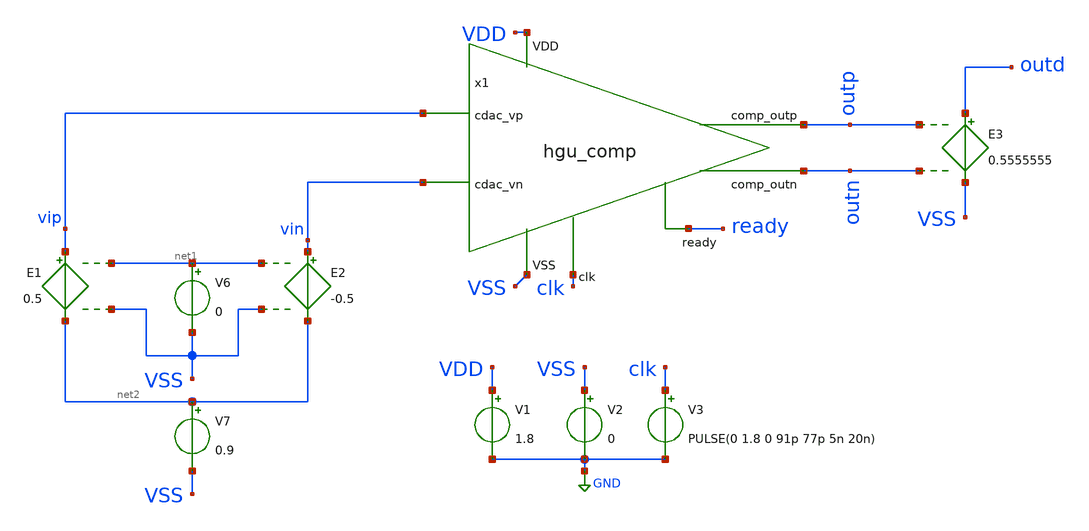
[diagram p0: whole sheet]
** sch_path: hgu/tb/tb_hgu_comp_MC_sim.sch
**.subckt tb_hgu_comp_MC_sim
x1 ready vin outp outn vip clk VDD VSS hgu_comp
V1 VDD GND 1.8
V2 VSS GND 0
V3 clk GND PULSE(0 1.8 0 91p 77p 5n 20n)
E1 vip net2 net1 VSS 0.5
E2 vin net2 net1 VSS -0.5
V6 net1 VSS 0
V7 net2 VSS 0.9
E3 outd VSS outp outn 0.5555555
**** begin user architecture code



.include /foss/designs/hgu_goss/hgu/spice/hgu_comp_flat_RC.spice
.lib /foss/pdks/sky130A/libs.tech/ngspice/sky130.lib.spice tt_mm
.include /foss/pdks/sky130A/libs.ref/sky130_fd_sc_hd/spice/sky130_fd_sc_hd.spice
.tran 0.1ns 100ns
.temp 25
.control
    repeat 20

    tran 0.1ns 100ns
    write test_mc_model.txt
    set appendwrite
    print V(outd)
    reset

    end
    plot all.v(outd)
.endc
.save all
.save all


**** end user architecture code
**.ends

* expanding   symbol:  ../xschem/hgu_comp.sym # of pins=8
** sym_path: hgu/xschem/hgu_comp.sym
** sch_path: hgu/xschem/hgu_comp.sch
.subckt hgu_comp ready cdac_vn comp_outp comp_outn cdac_vp clk VDD VSS
*.ipin cdac_vn
*.ipin cdac_vp
*.ipin VSS
*.ipin VDD
*.ipin clk
*.opin ready
*.opin comp_outp
*.opin comp_outn
XM1 net1 clk VSS VSS sky130_fd_pr__nfet_01v8 L=0.15 W=4 nf=4 ad='int((nf+1)/2) * W/nf * 0.29' as='int((nf+2)/2) * W/nf * 0.29'
+ pd='2*int((nf+1)/2) * (W/nf + 0.29)' ps='2*int((nf+2)/2) * (W/nf + 0.29)' nrd='0.29 / W' nrs='0.29 / W'
+ sa=0 sb=0 sd=0 mult=1 m=1
XM4 Y X Q VSS sky130_fd_pr__nfet_01v8 L=0.15 W=1 nf=1 ad='int((nf+1)/2) * W/nf * 0.29' as='int((nf+2)/2) * W/nf * 0.29'
+ pd='2*int((nf+1)/2) * (W/nf + 0.29)' ps='2*int((nf+2)/2) * (W/nf + 0.29)' nrd='0.29 / W' nrs='0.29 / W'
+ sa=0 sb=0 sd=0 mult=1 m=1
XM5 X Y P VSS sky130_fd_pr__nfet_01v8 L=0.15 W=1 nf=1 ad='int((nf+1)/2) * W/nf * 0.29' as='int((nf+2)/2) * W/nf * 0.29'
+ pd='2*int((nf+1)/2) * (W/nf + 0.29)' ps='2*int((nf+2)/2) * (W/nf + 0.29)' nrd='0.29 / W' nrs='0.29 / W'
+ sa=0 sb=0 sd=0 mult=1 m=1
XM6 X Y VDD VDD sky130_fd_pr__pfet_01v8 L=0.15 W=1 nf=1 ad='int((nf+1)/2) * W/nf * 0.29' as='int((nf+2)/2) * W/nf * 0.29'
+ pd='2*int((nf+1)/2) * (W/nf + 0.29)' ps='2*int((nf+2)/2) * (W/nf + 0.29)' nrd='0.29 / W' nrs='0.29 / W'
+ sa=0 sb=0 sd=0 mult=1 m=1
XM7 Y X VDD VDD sky130_fd_pr__pfet_01v8 L=0.15 W=1 nf=1 ad='int((nf+1)/2) * W/nf * 0.29' as='int((nf+2)/2) * W/nf * 0.29'
+ pd='2*int((nf+1)/2) * (W/nf + 0.29)' ps='2*int((nf+2)/2) * (W/nf + 0.29)' nrd='0.29 / W' nrs='0.29 / W'
+ sa=0 sb=0 sd=0 mult=1 m=1
XM8 X clk VDD VDD sky130_fd_pr__pfet_01v8 L=0.15 W=1 nf=1 ad='int((nf+1)/2) * W/nf * 0.29' as='int((nf+2)/2) * W/nf * 0.29'
+ pd='2*int((nf+1)/2) * (W/nf + 0.29)' ps='2*int((nf+2)/2) * (W/nf + 0.29)' nrd='0.29 / W' nrs='0.29 / W'
+ sa=0 sb=0 sd=0 mult=1 m=1
XM9 P clk VDD VDD sky130_fd_pr__pfet_01v8 L=0.15 W=1 nf=1 ad='int((nf+1)/2) * W/nf * 0.29' as='int((nf+2)/2) * W/nf * 0.29'
+ pd='2*int((nf+1)/2) * (W/nf + 0.29)' ps='2*int((nf+2)/2) * (W/nf + 0.29)' nrd='0.29 / W' nrs='0.29 / W'
+ sa=0 sb=0 sd=0 mult=1 m=1
XM10 Y clk VDD VDD sky130_fd_pr__pfet_01v8 L=0.15 W=1 nf=1 ad='int((nf+1)/2) * W/nf * 0.29' as='int((nf+2)/2) * W/nf * 0.29'
+ pd='2*int((nf+1)/2) * (W/nf + 0.29)' ps='2*int((nf+2)/2) * (W/nf + 0.29)' nrd='0.29 / W' nrs='0.29 / W'
+ sa=0 sb=0 sd=0 mult=1 m=1
XM11 Q clk VDD VDD sky130_fd_pr__pfet_01v8 L=0.15 W=1 nf=1 ad='int((nf+1)/2) * W/nf * 0.29' as='int((nf+2)/2) * W/nf * 0.29'
+ pd='2*int((nf+1)/2) * (W/nf + 0.29)' ps='2*int((nf+2)/2) * (W/nf + 0.29)' nrd='0.29 / W' nrs='0.29 / W'
+ sa=0 sb=0 sd=0 mult=1 m=1
XM16 RS_n RS_p VDD VDD sky130_fd_pr__pfet_01v8 L=0.15 W=0.84 nf=1 ad='int((nf+1)/2) * W/nf * 0.29' as='int((nf+2)/2) * W/nf * 0.29'
+ pd='2*int((nf+1)/2) * (W/nf + 0.29)' ps='2*int((nf+2)/2) * (W/nf + 0.29)' nrd='0.29 / W' nrs='0.29 / W'
+ sa=0 sb=0 sd=0 mult=1 m=1
XM17 RS_p RS_n VDD VDD sky130_fd_pr__pfet_01v8 L=0.15 W=0.84 nf=1 ad='int((nf+1)/2) * W/nf * 0.29' as='int((nf+2)/2) * W/nf * 0.29'
+ pd='2*int((nf+1)/2) * (W/nf + 0.29)' ps='2*int((nf+2)/2) * (W/nf + 0.29)' nrd='0.29 / W' nrs='0.29 / W'
+ sa=0 sb=0 sd=0 mult=1 m=1
XM19 RS_p Y_inv VSS VSS sky130_fd_pr__nfet_01v8 L=0.15 W=0.84 nf=1 ad='int((nf+1)/2) * W/nf * 0.29' as='int((nf+2)/2) * W/nf * 0.29'
+ pd='2*int((nf+1)/2) * (W/nf + 0.29)' ps='2*int((nf+2)/2) * (W/nf + 0.29)' nrd='0.29 / W' nrs='0.29 / W'
+ sa=0 sb=0 sd=0 mult=1 m=1
XM23 RS_n X_inv VSS VSS sky130_fd_pr__nfet_01v8 L=0.15 W=0.84 nf=1 ad='int((nf+1)/2) * W/nf * 0.29' as='int((nf+2)/2) * W/nf * 0.29'
+ pd='2*int((nf+1)/2) * (W/nf + 0.29)' ps='2*int((nf+2)/2) * (W/nf + 0.29)' nrd='0.29 / W' nrs='0.29 / W'
+ sa=0 sb=0 sd=0 mult=1 m=1
XM2 P cdac_vp net1 VSS sky130_fd_pr__nfet_01v8_lvt L=0.15 W=8 nf=8 ad='int((nf+1)/2) * W / nf * 0.29'
+ as='int((nf+2)/2) * W / nf * 0.29' pd='2*int((nf+1)/2) * (W / nf + 0.29)' ps='2*int((nf+2)/2) * (W / nf + 0.29)'
+ nrd='0.29 / W ' nrs='0.29 / W ' sa=0 sb=0 sd=0 mult=1 m=1
XM3 Q cdac_vn net1 VSS sky130_fd_pr__nfet_01v8_lvt L=0.15 W=8 nf=8 ad='int((nf+1)/2) * W / nf * 0.29'
+ as='int((nf+2)/2) * W / nf * 0.29' pd='2*int((nf+1)/2) * (W / nf + 0.29)' ps='2*int((nf+2)/2) * (W / nf + 0.29)'
+ nrd='0.29 / W ' nrs='0.29 / W ' sa=0 sb=0 sd=0 mult=1 m=1
XM12 X_inv X VDD VDD sky130_fd_pr__pfet_01v8 L=0.15 W=0.84 nf=1 ad='int((nf+1)/2) * W/nf * 0.29' as='int((nf+2)/2) * W/nf * 0.29'
+ pd='2*int((nf+1)/2) * (W/nf + 0.29)' ps='2*int((nf+2)/2) * (W/nf + 0.29)' nrd='0.29 / W' nrs='0.29 / W'
+ sa=0 sb=0 sd=0 mult=1 m=1
XM13 X_inv X VSS VSS sky130_fd_pr__nfet_01v8 L=0.15 W=0.42 nf=1 ad='int((nf+1)/2) * W/nf * 0.29' as='int((nf+2)/2) * W/nf * 0.29'
+ pd='2*int((nf+1)/2) * (W/nf + 0.29)' ps='2*int((nf+2)/2) * (W/nf + 0.29)' nrd='0.29 / W' nrs='0.29 / W'
+ sa=0 sb=0 sd=0 mult=1 m=1
XM14 X_drive X_inv VDD VDD sky130_fd_pr__pfet_01v8 L=0.15 W=2.52 nf=3 ad='int((nf+1)/2) * W/nf * 0.29'
+ as='int((nf+2)/2) * W/nf * 0.29' pd='2*int((nf+1)/2) * (W/nf + 0.29)' ps='2*int((nf+2)/2) * (W/nf + 0.29)'
+ nrd='0.29 / W' nrs='0.29 / W' sa=0 sb=0 sd=0 mult=1 m=1
XM15 X_drive X_inv VSS VSS sky130_fd_pr__nfet_01v8 L=0.15 W=1.38 nf=3 ad='int((nf+1)/2) * W/nf * 0.29'
+ as='int((nf+2)/2) * W/nf * 0.29' pd='2*int((nf+1)/2) * (W/nf + 0.29)' ps='2*int((nf+2)/2) * (W/nf + 0.29)'
+ nrd='0.29 / W' nrs='0.29 / W' sa=0 sb=0 sd=0 mult=1 m=1
XM18 Y_inv Y VDD VDD sky130_fd_pr__pfet_01v8 L=0.15 W=0.84 nf=1 ad='int((nf+1)/2) * W/nf * 0.29' as='int((nf+2)/2) * W/nf * 0.29'
+ pd='2*int((nf+1)/2) * (W/nf + 0.29)' ps='2*int((nf+2)/2) * (W/nf + 0.29)' nrd='0.29 / W' nrs='0.29 / W'
+ sa=0 sb=0 sd=0 mult=1 m=1
XM20 Y_inv Y VSS VSS sky130_fd_pr__nfet_01v8 L=0.15 W=0.42 nf=1 ad='int((nf+1)/2) * W/nf * 0.29' as='int((nf+2)/2) * W/nf * 0.29'
+ pd='2*int((nf+1)/2) * (W/nf + 0.29)' ps='2*int((nf+2)/2) * (W/nf + 0.29)' nrd='0.29 / W' nrs='0.29 / W'
+ sa=0 sb=0 sd=0 mult=1 m=1
XM21 Y_drive Y_inv VDD VDD sky130_fd_pr__pfet_01v8 L=0.15 W=2.52 nf=3 ad='int((nf+1)/2) * W/nf * 0.29'
+ as='int((nf+2)/2) * W/nf * 0.29' pd='2*int((nf+1)/2) * (W/nf + 0.29)' ps='2*int((nf+2)/2) * (W/nf + 0.29)'
+ nrd='0.29 / W' nrs='0.29 / W' sa=0 sb=0 sd=0 mult=1 m=1
XM22 Y_drive Y_inv VSS VSS sky130_fd_pr__nfet_01v8 L=0.15 W=1.38 nf=3 ad='int((nf+1)/2) * W/nf * 0.29'
+ as='int((nf+2)/2) * W/nf * 0.29' pd='2*int((nf+1)/2) * (W/nf + 0.29)' ps='2*int((nf+2)/2) * (W/nf + 0.29)'
+ nrd='0.29 / W' nrs='0.29 / W' sa=0 sb=0 sd=0 mult=1 m=1
XM24 net2 Y_drive X_drive VDD sky130_fd_pr__pfet_01v8 L=0.15 W=0.84 nf=1 ad='int((nf+1)/2) * W/nf * 0.29'
+ as='int((nf+2)/2) * W/nf * 0.29' pd='2*int((nf+1)/2) * (W/nf + 0.29)' ps='2*int((nf+2)/2) * (W/nf + 0.29)'
+ nrd='0.29 / W' nrs='0.29 / W' sa=0 sb=0 sd=0 mult=1 m=1
XM25 net2 X_drive Y_drive VDD sky130_fd_pr__pfet_01v8 L=0.15 W=0.84 nf=1 ad='int((nf+1)/2) * W/nf * 0.29'
+ as='int((nf+2)/2) * W/nf * 0.29' pd='2*int((nf+1)/2) * (W/nf + 0.29)' ps='2*int((nf+2)/2) * (W/nf + 0.29)'
+ nrd='0.29 / W' nrs='0.29 / W' sa=0 sb=0 sd=0 mult=1 m=1
XM26 net2 Y_drive net3 VSS sky130_fd_pr__nfet_01v8 L=0.15 W=0.84 nf=1 ad='int((nf+1)/2) * W/nf * 0.29'
+ as='int((nf+2)/2) * W/nf * 0.29' pd='2*int((nf+1)/2) * (W/nf + 0.29)' ps='2*int((nf+2)/2) * (W/nf + 0.29)'
+ nrd='0.29 / W' nrs='0.29 / W' sa=0 sb=0 sd=0 mult=1 m=1
XM27 net3 X_drive VSS VSS sky130_fd_pr__nfet_01v8 L=0.15 W=0.84 nf=1 ad='int((nf+1)/2) * W/nf * 0.29'
+ as='int((nf+2)/2) * W/nf * 0.29' pd='2*int((nf+1)/2) * (W/nf + 0.29)' ps='2*int((nf+2)/2) * (W/nf + 0.29)'
+ nrd='0.29 / W' nrs='0.29 / W' sa=0 sb=0 sd=0 mult=1 m=1
XM28 ready net2 VDD VDD sky130_fd_pr__pfet_01v8 L=0.15 W=0.84 nf=1 ad='int((nf+1)/2) * W/nf * 0.29' as='int((nf+2)/2) * W/nf * 0.29'
+ pd='2*int((nf+1)/2) * (W/nf + 0.29)' ps='2*int((nf+2)/2) * (W/nf + 0.29)' nrd='0.29 / W' nrs='0.29 / W'
+ sa=0 sb=0 sd=0 mult=1 m=1
XM29 ready net2 VSS VSS sky130_fd_pr__nfet_01v8 L=0.15 W=0.42 nf=1 ad='int((nf+1)/2) * W/nf * 0.29' as='int((nf+2)/2) * W/nf * 0.29'
+ pd='2*int((nf+1)/2) * (W/nf + 0.29)' ps='2*int((nf+2)/2) * (W/nf + 0.29)' nrd='0.29 / W' nrs='0.29 / W'
+ sa=0 sb=0 sd=0 mult=1 m=1
XM30 net4 RS_p VDD VDD sky130_fd_pr__pfet_01v8 L=0.15 W=0.84 nf=1 ad='int((nf+1)/2) * W/nf * 0.29' as='int((nf+2)/2) * W/nf * 0.29'
+ pd='2*int((nf+1)/2) * (W/nf + 0.29)' ps='2*int((nf+2)/2) * (W/nf + 0.29)' nrd='0.29 / W' nrs='0.29 / W'
+ sa=0 sb=0 sd=0 mult=1 m=1
XM31 net4 RS_p VSS VSS sky130_fd_pr__nfet_01v8 L=0.15 W=0.42 nf=1 ad='int((nf+1)/2) * W/nf * 0.29' as='int((nf+2)/2) * W/nf * 0.29'
+ pd='2*int((nf+1)/2) * (W/nf + 0.29)' ps='2*int((nf+2)/2) * (W/nf + 0.29)' nrd='0.29 / W' nrs='0.29 / W'
+ sa=0 sb=0 sd=0 mult=1 m=1
XM32 comp_outp net4 VDD VDD sky130_fd_pr__pfet_01v8 L=0.15 W=2.52 nf=3 ad='int((nf+1)/2) * W/nf * 0.29'
+ as='int((nf+2)/2) * W/nf * 0.29' pd='2*int((nf+1)/2) * (W/nf + 0.29)' ps='2*int((nf+2)/2) * (W/nf + 0.29)'
+ nrd='0.29 / W' nrs='0.29 / W' sa=0 sb=0 sd=0 mult=1 m=1
XM33 comp_outp net4 VSS VSS sky130_fd_pr__nfet_01v8 L=0.15 W=1.38 nf=3 ad='int((nf+1)/2) * W/nf * 0.29'
+ as='int((nf+2)/2) * W/nf * 0.29' pd='2*int((nf+1)/2) * (W/nf + 0.29)' ps='2*int((nf+2)/2) * (W/nf + 0.29)'
+ nrd='0.29 / W' nrs='0.29 / W' sa=0 sb=0 sd=0 mult=1 m=1
XM34 net5 RS_n VDD VDD sky130_fd_pr__pfet_01v8 L=0.15 W=0.84 nf=1 ad='int((nf+1)/2) * W/nf * 0.29' as='int((nf+2)/2) * W/nf * 0.29'
+ pd='2*int((nf+1)/2) * (W/nf + 0.29)' ps='2*int((nf+2)/2) * (W/nf + 0.29)' nrd='0.29 / W' nrs='0.29 / W'
+ sa=0 sb=0 sd=0 mult=1 m=1
XM35 net5 RS_n VSS VSS sky130_fd_pr__nfet_01v8 L=0.15 W=0.42 nf=1 ad='int((nf+1)/2) * W/nf * 0.29' as='int((nf+2)/2) * W/nf * 0.29'
+ pd='2*int((nf+1)/2) * (W/nf + 0.29)' ps='2*int((nf+2)/2) * (W/nf + 0.29)' nrd='0.29 / W' nrs='0.29 / W'
+ sa=0 sb=0 sd=0 mult=1 m=1
XM36 comp_outn net5 VDD VDD sky130_fd_pr__pfet_01v8 L=0.15 W=2.52 nf=3 ad='int((nf+1)/2) * W/nf * 0.29'
+ as='int((nf+2)/2) * W/nf * 0.29' pd='2*int((nf+1)/2) * (W/nf + 0.29)' ps='2*int((nf+2)/2) * (W/nf + 0.29)'
+ nrd='0.29 / W' nrs='0.29 / W' sa=0 sb=0 sd=0 mult=1 m=1
XM37 comp_outn net5 VSS VSS sky130_fd_pr__nfet_01v8 L=0.15 W=1.38 nf=3 ad='int((nf+1)/2) * W/nf * 0.29'
+ as='int((nf+2)/2) * W/nf * 0.29' pd='2*int((nf+1)/2) * (W/nf + 0.29)' ps='2*int((nf+2)/2) * (W/nf + 0.29)'
+ nrd='0.29 / W' nrs='0.29 / W' sa=0 sb=0 sd=0 mult=1 m=1
.ends

.GLOBAL GND
.end
